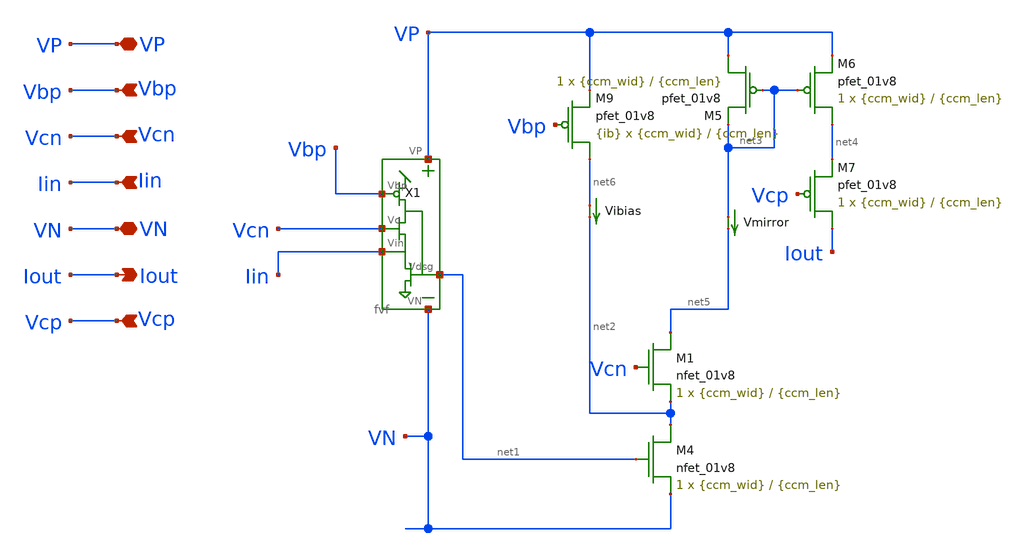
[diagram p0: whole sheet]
** sch_path: fvfccm.sch
**.subckt fvfccm Vbp Vcn Iin VP VN Iout Vcp
*.ipin Vbp
*.ipin Vcn
*.ipin Iin
*.iopin VP
*.iopin VN
*.opin Iout
*.ipin Vcp
XM4 net2 net1 VN VN sky130_fd_pr__nfet_01v8 L={ccm_len} W={ccm_wid} nf=1 ad='int((nf+1)/2) * W/nf * 0.29'
+ as='int((nf+2)/2) * W/nf * 0.29' pd='2*int((nf+1)/2) * (W/nf + 0.29)' ps='2*int((nf+2)/2) * (W/nf + 0.29)'
+ nrd='0.29 / W' nrs='0.29 / W' sa=0 sb=0 sd=0 mult=1 m=1
XM5 VP net3 net3 VP sky130_fd_pr__pfet_01v8 L={ccm_len} W={ccm_wid} nf=1 ad='int((nf+1)/2) * W/nf * 0.29'
+ as='int((nf+2)/2) * W/nf * 0.29' pd='2*int((nf+1)/2) * (W/nf + 0.29)' ps='2*int((nf+2)/2) * (W/nf + 0.29)'
+ nrd='0.29 / W' nrs='0.29 / W' sa=0 sb=0 sd=0 mult=1 m=1
XM6 net4 net3 VP VP sky130_fd_pr__pfet_01v8 L={ccm_len} W={ccm_wid} nf=1 ad='int((nf+1)/2) * W/nf * 0.29'
+ as='int((nf+2)/2) * W/nf * 0.29' pd='2*int((nf+1)/2) * (W/nf + 0.29)' ps='2*int((nf+2)/2) * (W/nf + 0.29)'
+ nrd='0.29 / W' nrs='0.29 / W' sa=0 sb=0 sd=0 mult=1 m=1
XM7 Iout Vcp net4 VP sky130_fd_pr__pfet_01v8 L={ccm_len} W={ccm_wid} nf=1 ad='int((nf+1)/2) * W/nf * 0.29'
+ as='int((nf+2)/2) * W/nf * 0.29' pd='2*int((nf+1)/2) * (W/nf + 0.29)' ps='2*int((nf+2)/2) * (W/nf + 0.29)'
+ nrd='0.29 / W' nrs='0.29 / W' sa=0 sb=0 sd=0 mult=1 m=1
XM9 net6 Vbp VP VP sky130_fd_pr__pfet_01v8 L={ccm_len} W={ccm_wid} nf=1 ad='int((nf+1)/2) * W/nf * 0.29'
+ as='int((nf+2)/2) * W/nf * 0.29' pd='2*int((nf+1)/2) * (W/nf + 0.29)' ps='2*int((nf+2)/2) * (W/nf + 0.29)'
+ nrd='0.29 / W' nrs='0.29 / W' sa=0 sb=0 sd=0 mult={ib} m={ib}
X1 VP Vbp Vcn Iin net1 VN fvf
Vmirror net3 net5 0
.save i(vmirror)
Vibias net6 net2 0
.save i(vibias)
XM1 net5 Vcn net2 VN sky130_fd_pr__nfet_01v8 L={ccm_len} W={ccm_wid} nf=1 ad='int((nf+1)/2) * W/nf * 0.29'
+ as='int((nf+2)/2) * W/nf * 0.29' pd='2*int((nf+1)/2) * (W/nf + 0.29)' ps='2*int((nf+2)/2) * (W/nf + 0.29)'
+ nrd='0.29 / W' nrs='0.29 / W' sa=0 sb=0 sd=0 mult=1 m=1
**.ends

* expanding   symbol:  fvf.sym # of pins=6
** sym_path: fvf.sym
** sch_path: fvf.sch
.subckt fvf VP Vbp Vc Vin Vdsg VN
*.iopin VP
*.ipin Vbp
*.ipin Vc
*.ipin Vin
*.iopin VN
*.opin Vdsg
XM3 Vdsg Vc Vin VN sky130_fd_pr__nfet_01v8 L={fvf_len} W={fvf_wid} nf=1 ad='int((nf+1)/2) * W/nf * 0.29'
+ as='int((nf+2)/2) * W/nf * 0.29' pd='2*int((nf+1)/2) * (W/nf + 0.29)' ps='2*int((nf+2)/2) * (W/nf + 0.29)'
+ nrd='0.29 / W' nrs='0.29 / W' sa=0 sb=0 sd=0 mult=1 m=1
XM4 VN Vdsg Vin VN sky130_fd_pr__nfet_01v8 L={fvf_len} W={fvf_wid} nf=1 ad='int((nf+1)/2) * W/nf * 0.29'
+ as='int((nf+2)/2) * W/nf * 0.29' pd='2*int((nf+1)/2) * (W/nf + 0.29)' ps='2*int((nf+2)/2) * (W/nf + 0.29)'
+ nrd='0.29 / W' nrs='0.29 / W' sa=0 sb=0 sd=0 mult=1 m=1
XM1 Vdsg Vbp VP VP sky130_fd_pr__pfet_01v8 L={fvf_len} W={fvf_wid} nf=1 ad='int((nf+1)/2) * W/nf * 0.29'
+ as='int((nf+2)/2) * W/nf * 0.29' pd='2*int((nf+1)/2) * (W/nf + 0.29)' ps='2*int((nf+2)/2) * (W/nf + 0.29)'
+ nrd='0.29 / W' nrs='0.29 / W' sa=0 sb=0 sd=0 mult={ib} m={ib}
.ends

.end
